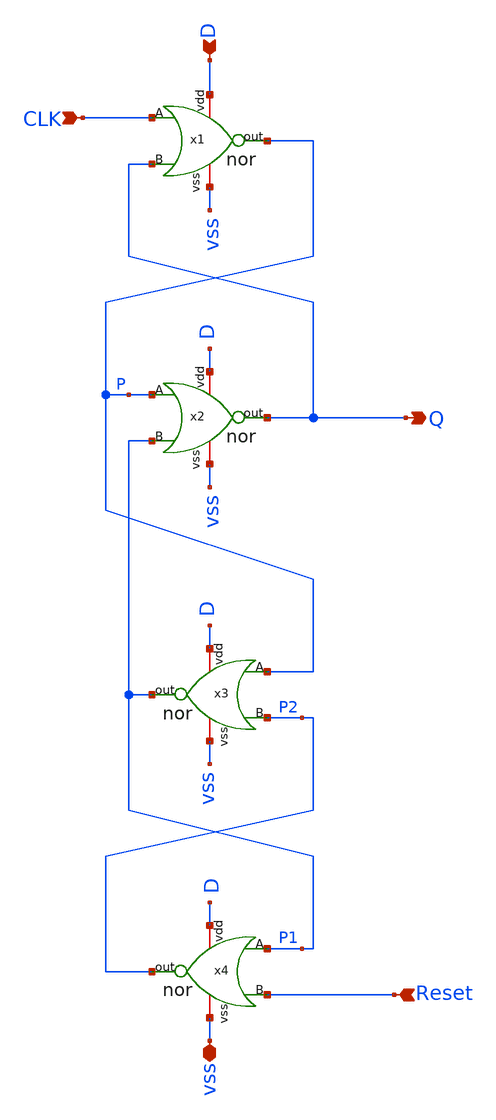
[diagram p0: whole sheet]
** sch_path: xschem/DFF.sch
**.subckt DFF D CLK Q Reset vss
*.ipin D
*.ipin CLK
*.opin Q
*.ipin Reset
*.iopin vss
x1 D CLK Q P vss nor
x2 D P P1 Q vss nor
x3 D P P2 P1 vss nor
x4 D P1 Reset P2 vss nor
**.ends

* expanding   symbol:  nor.sym # of pins=5
** sym_path: xschem/nor.sym
** sch_path: xschem/nor.sch
.subckt nor vdd A B out vss
*.ipin A
*.ipin B
*.iopin vdd
*.opin out
*.iopin vss
XM1 out A vss vss sky130_fd_pr__nfet_01v8 L=0.15 W=0.45 nf=1 ad='int((nf+1)/2) * W/nf * 0.29' as='int((nf+2)/2) * W/nf * 0.29'
+ pd='2*int((nf+1)/2) * (W/nf + 0.29)' ps='2*int((nf+2)/2) * (W/nf + 0.29)' nrd='0.29 / W' nrs='0.29 / W'
+ sa=0 sb=0 sd=0 mult=1 m=1
XM2 out B vss vss sky130_fd_pr__nfet_01v8 L=0.15 W=0.45 nf=1 ad='int((nf+1)/2) * W/nf * 0.29' as='int((nf+2)/2) * W/nf * 0.29'
+ pd='2*int((nf+1)/2) * (W/nf + 0.29)' ps='2*int((nf+2)/2) * (W/nf + 0.29)' nrd='0.29 / W' nrs='0.29 / W'
+ sa=0 sb=0 sd=0 mult=1 m=1
XM4 out B net1 vdd sky130_fd_pr__pfet_01v8 L=0.15 W=0.9 nf=1 ad='int((nf+1)/2) * W/nf * 0.29' as='int((nf+2)/2) * W/nf * 0.29'
+ pd='2*int((nf+1)/2) * (W/nf + 0.29)' ps='2*int((nf+2)/2) * (W/nf + 0.29)' nrd='0.29 / W' nrs='0.29 / W'
+ sa=0 sb=0 sd=0 mult=1 m=1
XM3 net1 A vdd vdd sky130_fd_pr__pfet_01v8 L=0.15 W=0.9 nf=1 ad='int((nf+1)/2) * W/nf * 0.29' as='int((nf+2)/2) * W/nf * 0.29'
+ pd='2*int((nf+1)/2) * (W/nf + 0.29)' ps='2*int((nf+2)/2) * (W/nf + 0.29)' nrd='0.29 / W' nrs='0.29 / W'
+ sa=0 sb=0 sd=0 mult=1 m=1
XM5 net2 B vdd vdd sky130_fd_pr__pfet_01v8 L=0.15 W=0.9 nf=1 ad='int((nf+1)/2) * W/nf * 0.29' as='int((nf+2)/2) * W/nf * 0.29'
+ pd='2*int((nf+1)/2) * (W/nf + 0.29)' ps='2*int((nf+2)/2) * (W/nf + 0.29)' nrd='0.29 / W' nrs='0.29 / W'
+ sa=0 sb=0 sd=0 mult=1 m=1
XM6 out A net2 vdd sky130_fd_pr__pfet_01v8 L=0.15 W=0.9 nf=1 ad='int((nf+1)/2) * W/nf * 0.29' as='int((nf+2)/2) * W/nf * 0.29'
+ pd='2*int((nf+1)/2) * (W/nf + 0.29)' ps='2*int((nf+2)/2) * (W/nf + 0.29)' nrd='0.29 / W' nrs='0.29 / W'
+ sa=0 sb=0 sd=0 mult=1 m=1
.ends

.end
